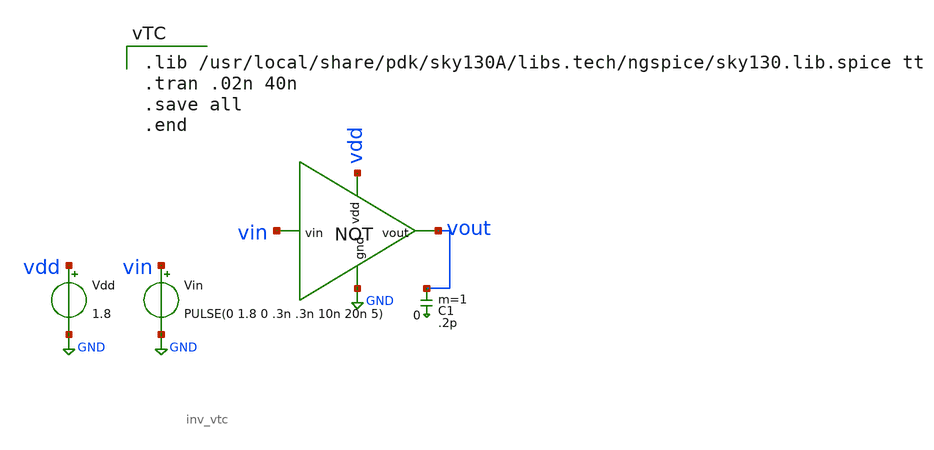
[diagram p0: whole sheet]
** sch_path: inv_test.sch
**.subckt inv_test
x1 vout vdd GND vin inv_vtc
Vin vin GND PULSE(0 1.8 0 .3n .3n 10n 20n 5)
Vdd vdd GND 1.8
C1 vout 0 .2p m=1
**** begin user architecture code

.lib /usr/local/share/pdk/sky130A/libs.tech/ngspice/sky130.lib.spice tt
.tran .02n 40n
.save all
.end

**** end user architecture code
**.ends

* expanding   symbol:  inv_vtc.sym # of pins=4
** sym_path: inv_vtc.sym
** sch_path: inv_vtc.sch
.subckt inv_vtc vout vdd gnd vin
*.ipin vin
*.ipin vdd
*.ipin gnd
*.opin vout
XM1 vout vin gnd gnd sky130_fd_pr__nfet_01v8 L=0.15 W=1 nf=1 ad='int((nf+1)/2) * W/nf * 0.29' as='int((nf+2)/2) * W/nf * 0.29'
+ pd='2*int((nf+1)/2) * (W/nf + 0.29)' ps='2*int((nf+2)/2) * (W/nf + 0.29)' nrd='0.29 / W' nrs='0.29 / W'
+ sa=0 sb=0 sd=0 mult=1 m=1
XM2 vout vin vdd vdd sky130_fd_pr__pfet_01v8 L=0.15 W=2 nf=1 ad='int((nf+1)/2) * W/nf * 0.29' as='int((nf+2)/2) * W/nf * 0.29'
+ pd='2*int((nf+1)/2) * (W/nf + 0.29)' ps='2*int((nf+2)/2) * (W/nf + 0.29)' nrd='0.29 / W' nrs='0.29 / W'
+ sa=0 sb=0 sd=0 mult=1 m=1
.ends

.GLOBAL GND
.end
